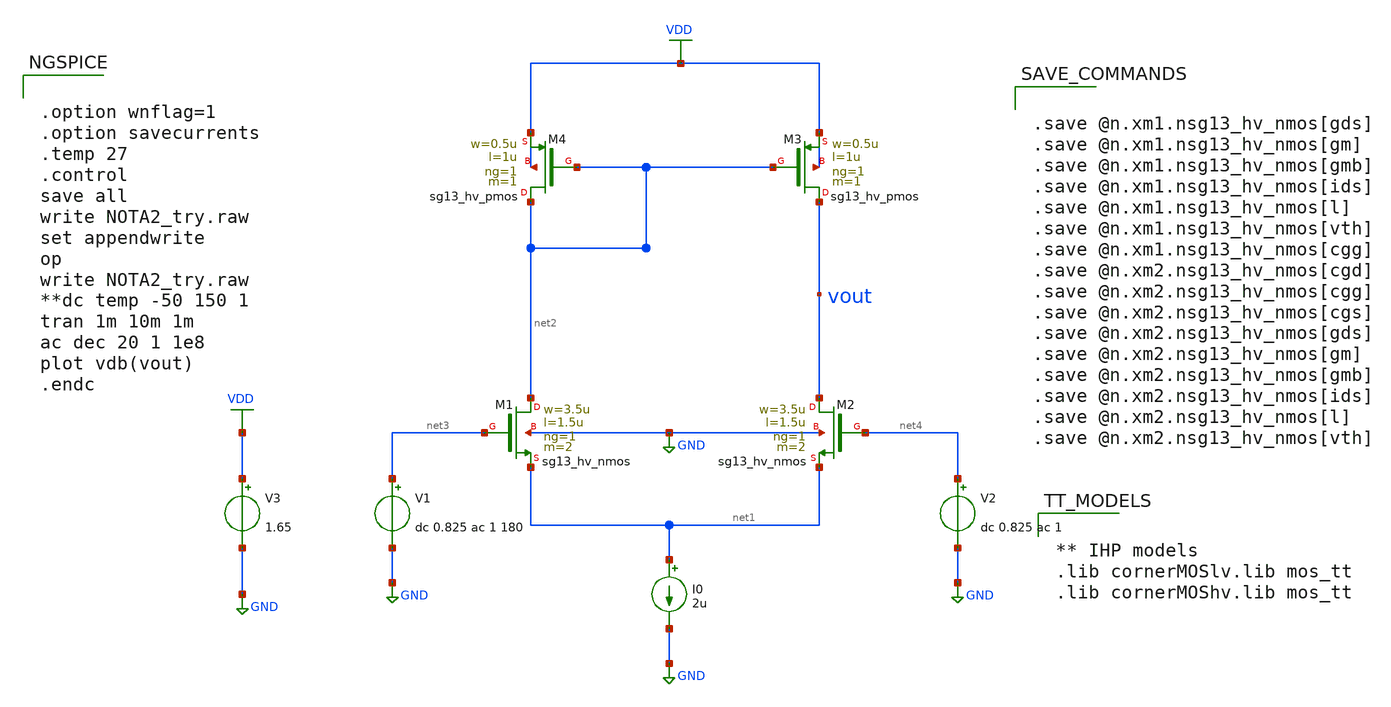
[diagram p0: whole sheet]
** sch_path: Design Files/RAMP/OTA/NOTA2_try.sch
**.subckt NOTA2_try
XM1 net2 net3 net1 GND sg13_hv_nmos w=3.5u l=1.5u ng=1 m=2 mm_ok=1
XM2 vout net4 net1 GND sg13_hv_nmos w=3.5u l=1.5u ng=1 m=2 mm_ok=1
I0 net1 GND 2u
XM3 vout net2 VDD VDD sg13_hv_pmos w=0.5u l=1u ng=1 m=1 mm_ok=1
XM4 net2 net2 VDD VDD sg13_hv_pmos w=0.5u l=1u ng=1 m=1 mm_ok=1
V1 net3 GND dc 0.825 ac 1 180
V2 net4 GND dc 0.825 ac 1
V3 VDD GND 1.65
**** begin user architecture code


.option wnflag=1
.option savecurrents
.temp 27
.control
save all
write NOTA2_try.raw
set appendwrite
op
write NOTA2_try.raw
**dc temp -50 150 1
tran 1m 10m 1m
ac dec 20 1 1e8
plot vdb(vout)
.endc




.save @n.xm1.nsg13_hv_nmos[gds]
.save @n.xm1.nsg13_hv_nmos[gm]
.save @n.xm1.nsg13_hv_nmos[gmb]
.save @n.xm1.nsg13_hv_nmos[ids]
.save @n.xm1.nsg13_hv_nmos[l]
.save @n.xm1.nsg13_hv_nmos[vth]
.save @n.xm1.nsg13_hv_nmos[cgg]
.save @n.xm2.nsg13_hv_nmos[cgd]
.save @n.xm2.nsg13_hv_nmos[cgg]
.save @n.xm2.nsg13_hv_nmos[cgs]
.save @n.xm2.nsg13_hv_nmos[gds]
.save @n.xm2.nsg13_hv_nmos[gm]
.save @n.xm2.nsg13_hv_nmos[gmb]
.save @n.xm2.nsg13_hv_nmos[ids]
.save @n.xm2.nsg13_hv_nmos[l]
.save @n.xm2.nsg13_hv_nmos[vth]




** IHP models
.lib cornerMOSlv.lib mos_tt
.lib cornerMOShv.lib mos_tt


**** end user architecture code
**.ends
.GLOBAL GND
.GLOBAL VDD
.end
